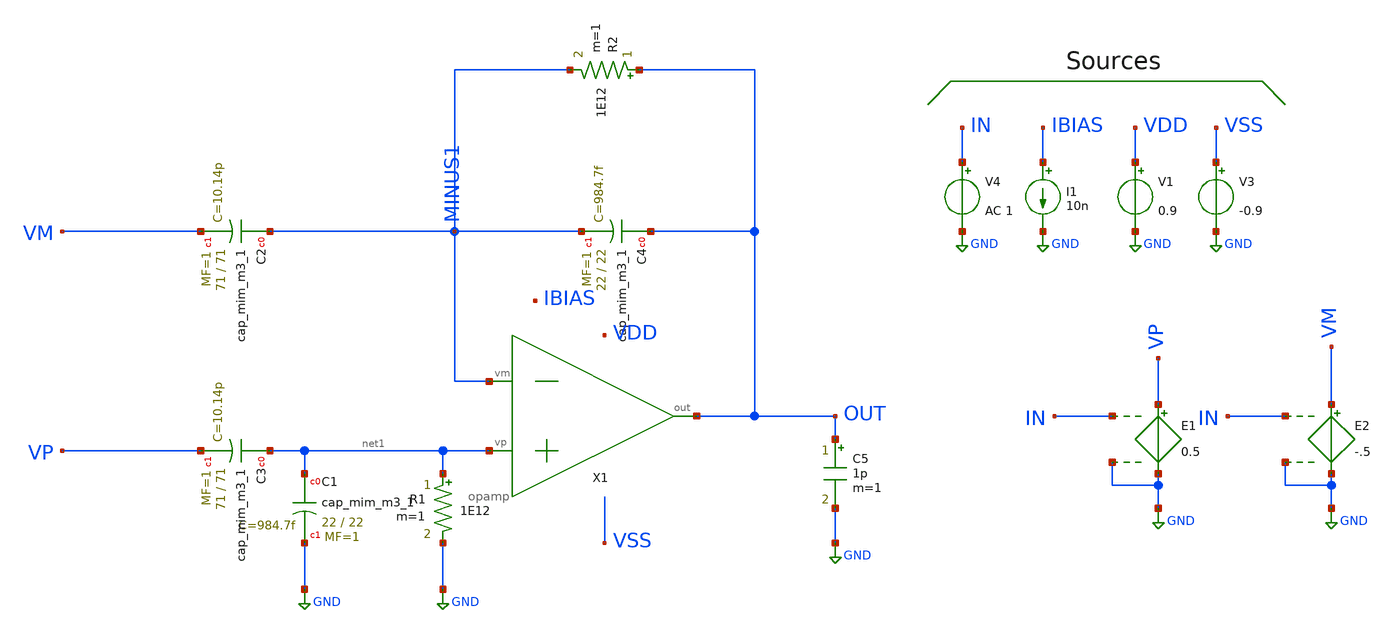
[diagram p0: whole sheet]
** sch_path: xschem/LNA/LNA_IDEAL_TB.sch
**.subckt LNA_IDEAL_TB
XC4 OUT MINUS1 sky130_fd_pr__cap_mim_m3_1 W=22 L=22 MF=1 m=1
XC2 MINUS1 VM sky130_fd_pr__cap_mim_m3_1 W=71 L=71 MF=1 m=1
R2 OUT MINUS1 1E12 m=1
XC1 net1 GND sky130_fd_pr__cap_mim_m3_1 W=22 L=22 MF=1 m=1
XC3 net1 VP sky130_fd_pr__cap_mim_m3_1 W=71 L=71 MF=1 m=1
R1 net1 GND 1E12 m=1
V1 VDD GND 0.9
V4 IN GND AC 1
V3 VSS GND -0.9
I1 IBIAS GND 10n
C5 OUT GND 1p m=1
E1 VP GND IN GND 0.5
E2 VM GND IN GND -.5
X1 net1 MINUS1 OUT opamp
**** begin user architecture code



*.include ~/OpenPDK/skywater-pdk/skywater-pdk/libraries/sky130_fd_pr/latest/cells/pfet_g5v0d10v5/sky130_fd_pr__pfet_g5v0d10v5__tt.corner.spice
*.include ~/OpenPDK/skywater-pdk/skywater-pdk/libraries/sky130_fd_pr/latest/cells/pfet_g5v0d10v5/sky130_fd_pr__pfet_g5v0d10v5__mismatch.corner.spice
*.include ~/OpenPDK/skywater-pdk/skywater-pdk/libraries/sky130_fd_pr/latest/cells/pfet_g5v0d10v5/sky130_fd_pr__nfet_g5v0d10v5__tt.corner.spice
*.include ~/OpenPDK/skywater-pdk/skywater-pdk/libraries/sky130_fd_pr/latest/cells/pfet_g5v0d10v5/sky130_fd_pr__nfet_g5v0d10v5__mismatch.corner.spice

.include /usr/share/pdk/sky130A/libs.ref/spi/sky130_fd_pr/sky130_fd_pr__nfet_01v8_lvt__tt.corner.spice
.include /usr/share/pdk/sky130A/libs.ref/spi/sky130_fd_pr/sky130_fd_pr__nfet_01v8_lvt__mismatch.corner.spice
.include /usr/share/pdk/sky130A/libs.ref/spi/sky130_fd_pr/sky130_fd_pr__pfet_01v8_lvt__tt.corner.spice
.include /usr/share/pdk/sky130A/libs.ref/spi/sky130_fd_pr/sky130_fd_pr__pfet_01v8_lvt__mismatch.corner.spice
*.include /usr/share/pdk/sky130A/libs.ref/spi/sky130_fd_pr/sky130_fd_pr__cap_mim_m3_1.model.spice



.include ~/OpenPDK/skywater-pdk/skywater-pdk/libraries/sky130_fd_pr/latest/models/all.spice
.include ~/OpenPDK/skywater-pdk/skywater-pdk/libraries/sky130_fd_pr/latest/models/sky130_fd_pr__model__r+c.model.spice
.include ~/OpenPDK/skywater-pdk/skywater-pdk/libraries/sky130_fd_pr/latest/models/r+c/res_typical__cap_typical.spice
.include ~/OpenPDK/skywater-pdk/skywater-pdk/libraries/sky130_fd_pr/latest/models/r+c/res_typical__cap_typical__lin.spice





.option gmin=1E-15

.control

******************OP Simulation*************************************
op
print OUT
print MINUS1
********************************************************************


*******************DC Simulation************************************
*dc V2 0.85 0.95 10u
*plot OUT
*plot deriv(OUT)
********************************************************************


********************AC Simulation***********************************
ac dec 100 0.01 1MEG
plot db(OUT)
********************************************************************


********************Transient Simulation****************************
*tran 1m 2
*plot VP VM OUT
********************************************************************

********************Noise Simulation********************************
*set sqrnoise
noise v(out) V4 dec 100 50m 100
*setplot noise1
*plot log(inoise_spectrum)
*plot onoise_spectrum

print inoise_total
*print onoise_total
********************************************************************
.endc


**** end user architecture code
**.ends

* expanding   symbol:  MISC/opamp.sym # of pins=3
** sym_path: xschem/MISC/opamp.sym
** sch_path: xschem/MISC/opamp.sch
.subckt opamp vp vm out
*.ipin vp
*.ipin vm
*.opin out
E1 out GND vp vm 1E6
.ends

.GLOBAL GND
.end
